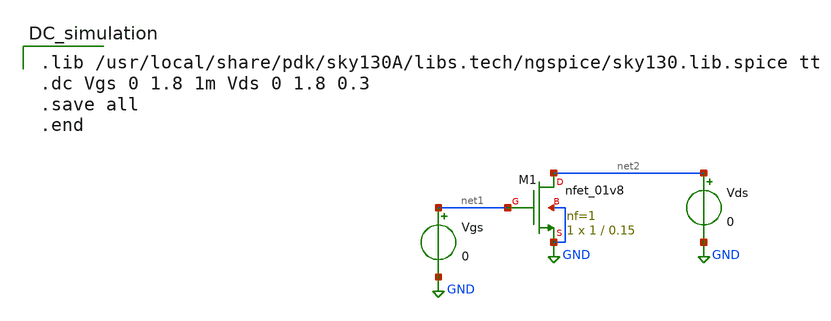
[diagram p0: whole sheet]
** sch_path: Design-and-analysis-of-CMOS-ineverter/XSCHEM FILES/NMOS.sch
**.subckt NMOS
XM1 net2 net1 GND GND sky130_fd_pr__nfet_01v8 L=0.15 W=1 nf=1 ad='int((nf+1)/2) * W/nf * 0.29' as='int((nf+2)/2) * W/nf * 0.29'
+ pd='2*int((nf+1)/2) * (W/nf + 0.29)' ps='2*int((nf+2)/2) * (W/nf + 0.29)' nrd='0.29 / W' nrs='0.29 / W'
+ sa=0 sb=0 sd=0 mult=1 m=1
Vgs net1 GND 0
Vds net2 GND 0
**** begin user architecture code

.lib /usr/local/share/pdk/sky130A/libs.tech/ngspice/sky130.lib.spice tt
.dc Vgs 0 1.8 1m Vds 0 1.8 0.3
.save all
.end

**** end user architecture code
**.ends
.GLOBAL GND
.end
